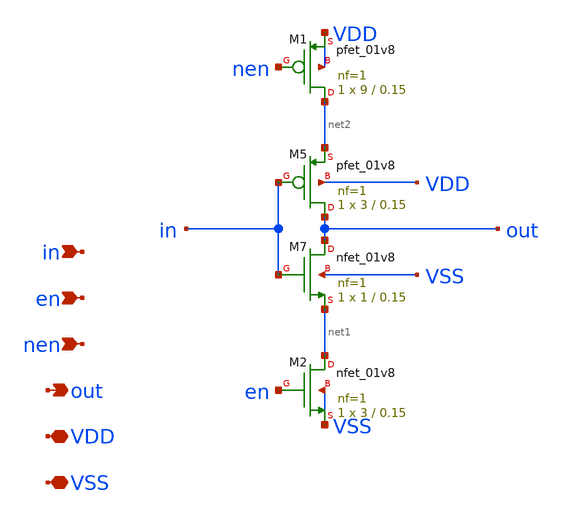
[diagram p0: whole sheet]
** sch_path: xschem/tristate_inverter.sch
**.subckt tristate_inverter VDD in out VSS en nen
*.iopin VDD
*.ipin in
*.opin out
*.iopin VSS
*.ipin en
*.ipin nen
XM5 out in net2 VDD sky130_fd_pr__pfet_01v8 L=0.15 W=3 nf=1 ad='int((nf+1)/2) * W/nf * 0.29' as='int((nf+2)/2) * W/nf * 0.29'
+ pd='2*int((nf+1)/2) * (W/nf + 0.29)' ps='2*int((nf+2)/2) * (W/nf + 0.29)' nrd='0.29 / W' nrs='0.29 / W'
+ sa=0 sb=0 sd=0 mult=1 m=1
XM7 out in net1 VSS sky130_fd_pr__nfet_01v8 L=0.15 W=1 nf=1 ad='int((nf+1)/2) * W/nf * 0.29' as='int((nf+2)/2) * W/nf * 0.29'
+ pd='2*int((nf+1)/2) * (W/nf + 0.29)' ps='2*int((nf+2)/2) * (W/nf + 0.29)' nrd='0.29 / W' nrs='0.29 / W'
+ sa=0 sb=0 sd=0 mult=1 m=1
XM1 net2 nen VDD VDD sky130_fd_pr__pfet_01v8 L=0.15 W=9 nf=1 ad='int((nf+1)/2) * W/nf * 0.29' as='int((nf+2)/2) * W/nf * 0.29'
+ pd='2*int((nf+1)/2) * (W/nf + 0.29)' ps='2*int((nf+2)/2) * (W/nf + 0.29)' nrd='0.29 / W' nrs='0.29 / W'
+ sa=0 sb=0 sd=0 mult=1 m=1
XM2 net1 en VSS VSS sky130_fd_pr__nfet_01v8 L=0.15 W=3 nf=1 ad='int((nf+1)/2) * W/nf * 0.29' as='int((nf+2)/2) * W/nf * 0.29'
+ pd='2*int((nf+1)/2) * (W/nf + 0.29)' ps='2*int((nf+2)/2) * (W/nf + 0.29)' nrd='0.29 / W' nrs='0.29 / W'
+ sa=0 sb=0 sd=0 mult=1 m=1
**.ends
.end
